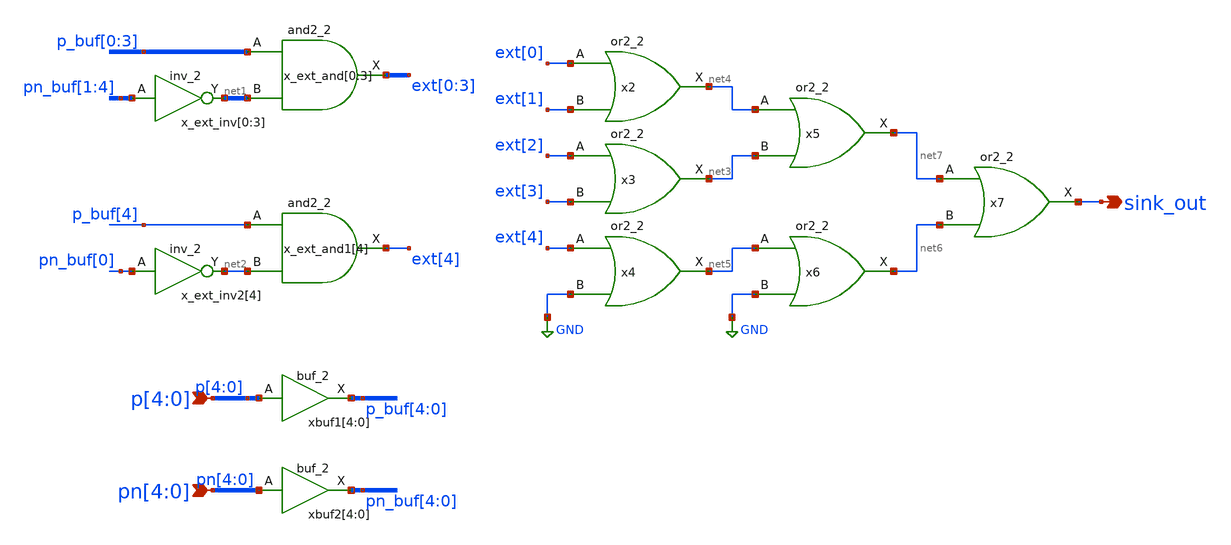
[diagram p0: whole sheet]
** sch_path: xschem/lib/phase_extractor.sch
**.subckt phase_extractor p[4],p[3],p[2],p[1],p[0] pn[4],pn[3],pn[2],pn[1],pn[0] sink_out
*.ipin p[4],p[3],p[2],p[1],p[0]
*.ipin pn[4],pn[3],pn[2],pn[1],pn[0]
*.opin sink_out
xbuf1[4] p[4] GND GND VDD VDD p_buf[4] sky130_fd_sc_hd__buf_2
xbuf1[3] p[3] GND GND VDD VDD p_buf[3] sky130_fd_sc_hd__buf_2
xbuf1[2] p[2] GND GND VDD VDD p_buf[2] sky130_fd_sc_hd__buf_2
xbuf1[1] p[1] GND GND VDD VDD p_buf[1] sky130_fd_sc_hd__buf_2
xbuf1[0] p[0] GND GND VDD VDD p_buf[0] sky130_fd_sc_hd__buf_2
xbuf2[4] pn[4] GND GND VDD VDD pn_buf[4] sky130_fd_sc_hd__buf_2
xbuf2[3] pn[3] GND GND VDD VDD pn_buf[3] sky130_fd_sc_hd__buf_2
xbuf2[2] pn[2] GND GND VDD VDD pn_buf[2] sky130_fd_sc_hd__buf_2
xbuf2[1] pn[1] GND GND VDD VDD pn_buf[1] sky130_fd_sc_hd__buf_2
xbuf2[0] pn[0] GND GND VDD VDD pn_buf[0] sky130_fd_sc_hd__buf_2
x_ext_and[0] p_buf[0] net1[3] GND GND VDD VDD ext[0] sky130_fd_sc_hd__and2_2
x_ext_and[1] p_buf[1] net1[2] GND GND VDD VDD ext[1] sky130_fd_sc_hd__and2_2
x_ext_and[2] p_buf[2] net1[1] GND GND VDD VDD ext[2] sky130_fd_sc_hd__and2_2
x_ext_and[3] p_buf[3] net1[0] GND GND VDD VDD ext[3] sky130_fd_sc_hd__and2_2
x_ext_inv[0] pn_buf[1] GND GND VDD VDD net1[3] sky130_fd_sc_hd__inv_2
x_ext_inv[1] pn_buf[2] GND GND VDD VDD net1[2] sky130_fd_sc_hd__inv_2
x_ext_inv[2] pn_buf[3] GND GND VDD VDD net1[1] sky130_fd_sc_hd__inv_2
x_ext_inv[3] pn_buf[4] GND GND VDD VDD net1[0] sky130_fd_sc_hd__inv_2
x_ext_and1[4] p_buf[4] net2 GND GND VDD VDD ext[4] sky130_fd_sc_hd__and2_2
x_ext_inv2[4] pn_buf[0] GND GND VDD VDD net2 sky130_fd_sc_hd__inv_2
x3 ext[2] ext[3] GND GND VDD VDD net3 sky130_fd_sc_hd__or2_2
x2 ext[0] ext[1] GND GND VDD VDD net4 sky130_fd_sc_hd__or2_2
x4 ext[4] GND GND GND VDD VDD net5 sky130_fd_sc_hd__or2_2
x5 net4 net3 GND GND VDD VDD net7 sky130_fd_sc_hd__or2_2
x6 net5 GND GND GND VDD VDD net6 sky130_fd_sc_hd__or2_2
x7 net7 net6 GND GND VDD VDD sink_out sky130_fd_sc_hd__or2_2
**.ends
.GLOBAL GND
.end
